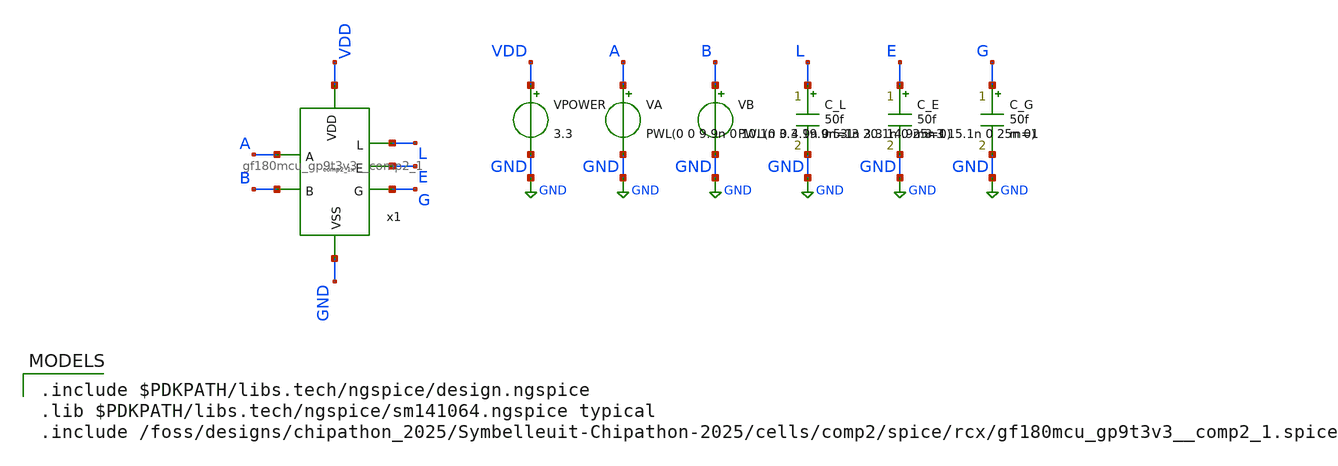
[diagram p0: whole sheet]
** sch_path: cells/comp2/cace/templates/comp2_tb_timing.sch
**.subckt comp2_tb_timing
x1 VDD L A E G B GND gf180mcu_gp9t3v3__comp2_1
VPOWER VDD GND 3.3
VA A GND PWL(0 0 9.9n 0 10.1n 3.3 19.9n 3.3 20.1n 0 25n 0)
VB B GND PWL(0 0 4.9n 0 5.1n 3.3 14.9n 3.3 15.1n 0 25n 0)
C_L L GND 50f m=1
C_E E GND 50f m=1
C_G G GND 50f m=1
**** begin user architecture code

.include $PDKPATH/libs.tech/ngspice/design.ngspice
.lib $PDKPATH/libs.tech/ngspice/sm141064.ngspice typical
.include /foss/designs/chipathon_2025/Symbelleuit-Chipathon-2025/cells/comp2/spice/rcx/gf180mcu_gp9t3v3__comp2_1.spice


* CACE Timing Propagation Delay Simulation
.tran 50p 25n
.control
  run
  meas tran tpd_L_LH trig v(B) val=1.65 rise=1 targ v(L) val=1.65 rise=1
  meas tran tpd_E_HL trig v(B) val=1.65 rise=1 targ v(E) val=1.65 fall=1
  meas tran tpd_L_HL trig v(A) val=1.65 rise=1 targ v(L) val=1.65 fall=1
  meas tran tpd_E_LH trig v(A) val=1.65 rise=1 targ v(E) val=1.65 rise=1
  meas tran tpd_G_LH trig v(B) val=1.65 fall=1 targ v(G) val=1.65 rise=1
  meas tran tpd_G_HL trig v(A) val=1.65 fall=1 targ v(G) val=1.65 fall=1
  let tpd_max = max(max(tpd_L_LH, tpd_L_HL), max(max(tpd_G_LH, tpd_G_HL), max(tpd_E_LH, tpd_E_HL)))
  print tpd_max
  echo $&tpd_max > comp2_tb_timing_0.data
.endc
.GLOBAL GND


**** end user architecture code
**.ends
.GLOBAL GND
.end
